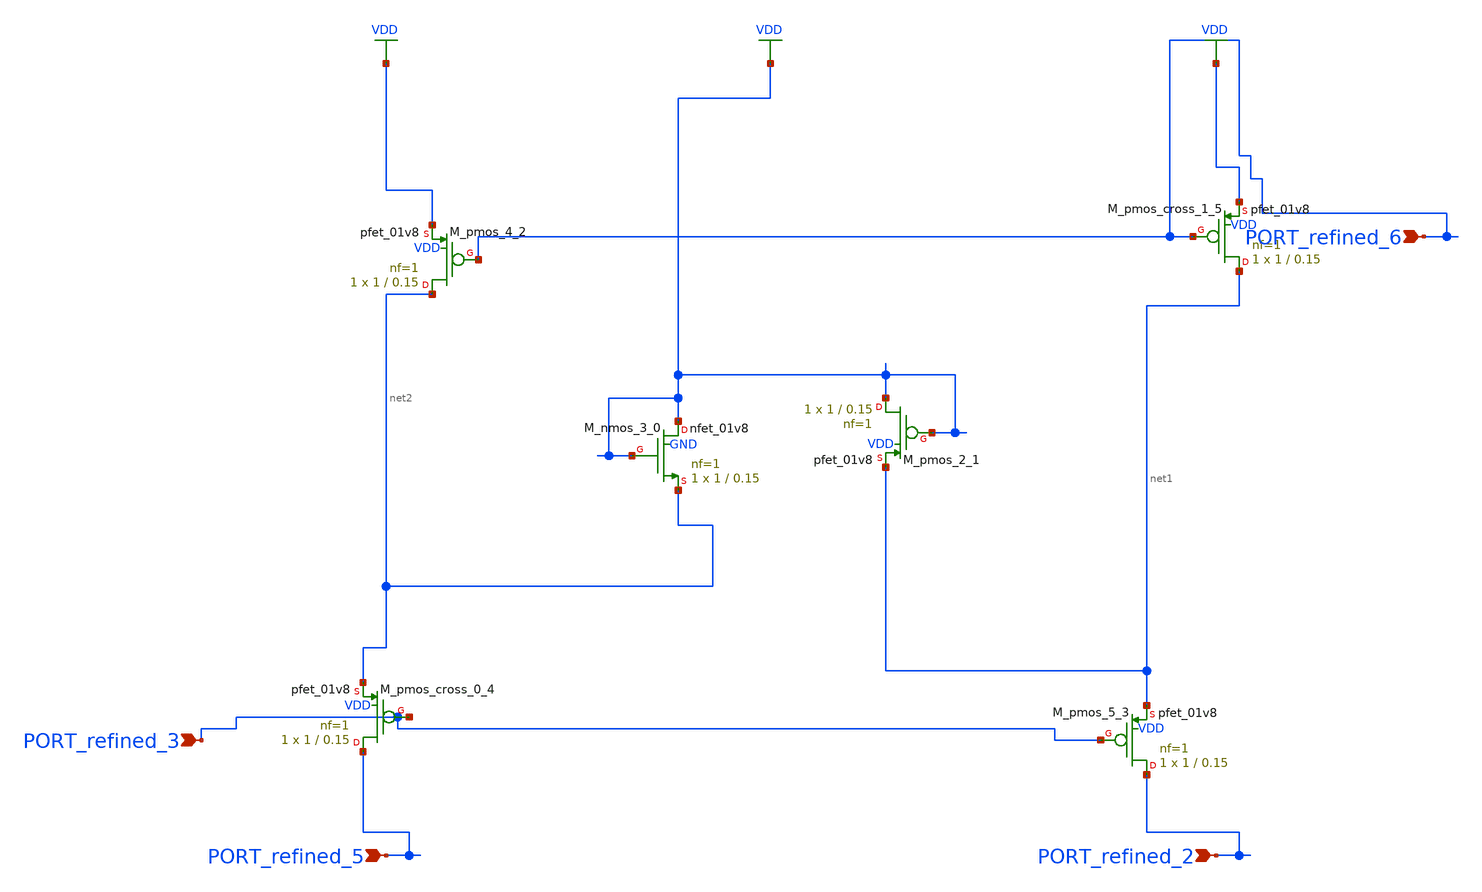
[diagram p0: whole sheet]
** sch_path: schematics/AMSNet/698.sch
**.subckt 698 PORT_refined_5 PORT_refined_6 PORT_refined_3 PORT_refined_2
*.ipin PORT_refined_5
*.ipin PORT_refined_6
*.ipin PORT_refined_3
*.ipin PORT_refined_2
XM_nmos_3_0 VDD VDD net2 GND sky130_fd_pr__nfet_01v8 L=0.15 W=1 nf=1 ad='int((1 + 1)/2) * 1 / 1 * 0.29'
+ as='int((1 + 2)/2) * 1 / 1 * 0.29' pd='2*int((1 + 1)/2) * (1 / 1 + 0.29)' ps='2*int((1 + 2)/2) * (1 / 1 + 0.29)'
+ nrd='0.29 / 1 ' nrs='0.29 / 1 ' sa=0 sb=0 sd=0 mult=1 m=1
XM_pmos_2_1 VDD VDD net1 VDD sky130_fd_pr__pfet_01v8 L=0.15 W=1 nf=1 ad='int((1 + 1)/2) * 1 / 1 * 0.29'
+ as='int((1 + 2)/2) * 1 / 1 * 0.29' pd='2*int((1 + 1)/2) * (1 / 1 + 0.29)' ps='2*int((1 + 2)/2) * (1 / 1 + 0.29)'
+ nrd='0.29 / 1 ' nrs='0.29 / 1 ' sa=0 sb=0 sd=0 mult=1 m=1
XM_pmos_4_2 net2 PORT_refined_6 VDD VDD sky130_fd_pr__pfet_01v8 L=0.15 W=1 nf=1 ad='int((1 + 1)/2) * 1 / 1 * 0.29'
+ as='int((1 + 2)/2) * 1 / 1 * 0.29' pd='2*int((1 + 1)/2) * (1 / 1 + 0.29)' ps='2*int((1 + 2)/2) * (1 / 1 + 0.29)'
+ nrd='0.29 / 1 ' nrs='0.29 / 1 ' sa=0 sb=0 sd=0 mult=1 m=1
XM_pmos_5_3 PORT_refined_2 PORT_refined_3 net1 VDD sky130_fd_pr__pfet_01v8 L=0.15 W=1 nf=1 ad='int((1 + 1)/2) * 1 / 1 * 0.29'
+ as='int((1 + 2)/2) * 1 / 1 * 0.29' pd='2*int((1 + 1)/2) * (1 / 1 + 0.29)' ps='2*int((1 + 2)/2) * (1 / 1 + 0.29)'
+ nrd='0.29 / 1 ' nrs='0.29 / 1 ' sa=0 sb=0 sd=0 mult=1 m=1
XM_pmos_cross_0_4 PORT_refined_5 PORT_refined_3 net2 VDD sky130_fd_pr__pfet_01v8 L=0.15 W=1 nf=1 ad='int((1 + 1)/2) * 1 / 1 * 0.29'
+ as='int((1 + 2)/2) * 1 / 1 * 0.29' pd='2*int((1 + 1)/2) * (1 / 1 + 0.29)' ps='2*int((1 + 2)/2) * (1 / 1 + 0.29)'
+ nrd='0.29 / 1 ' nrs='0.29 / 1 ' sa=0 sb=0 sd=0 mult=1 m=1
XM_pmos_cross_1_5 net1 PORT_refined_6 VDD VDD sky130_fd_pr__pfet_01v8 L=0.15 W=1 nf=1 ad='int((1 + 1)/2) * 1 / 1 * 0.29'
+ as='int((1 + 2)/2) * 1 / 1 * 0.29' pd='2*int((1 + 1)/2) * (1 / 1 + 0.29)' ps='2*int((1 + 2)/2) * (1 / 1 + 0.29)'
+ nrd='0.29 / 1 ' nrs='0.29 / 1 ' sa=0 sb=0 sd=0 mult=1 m=1
**.ends
.GLOBAL VDD
.end
